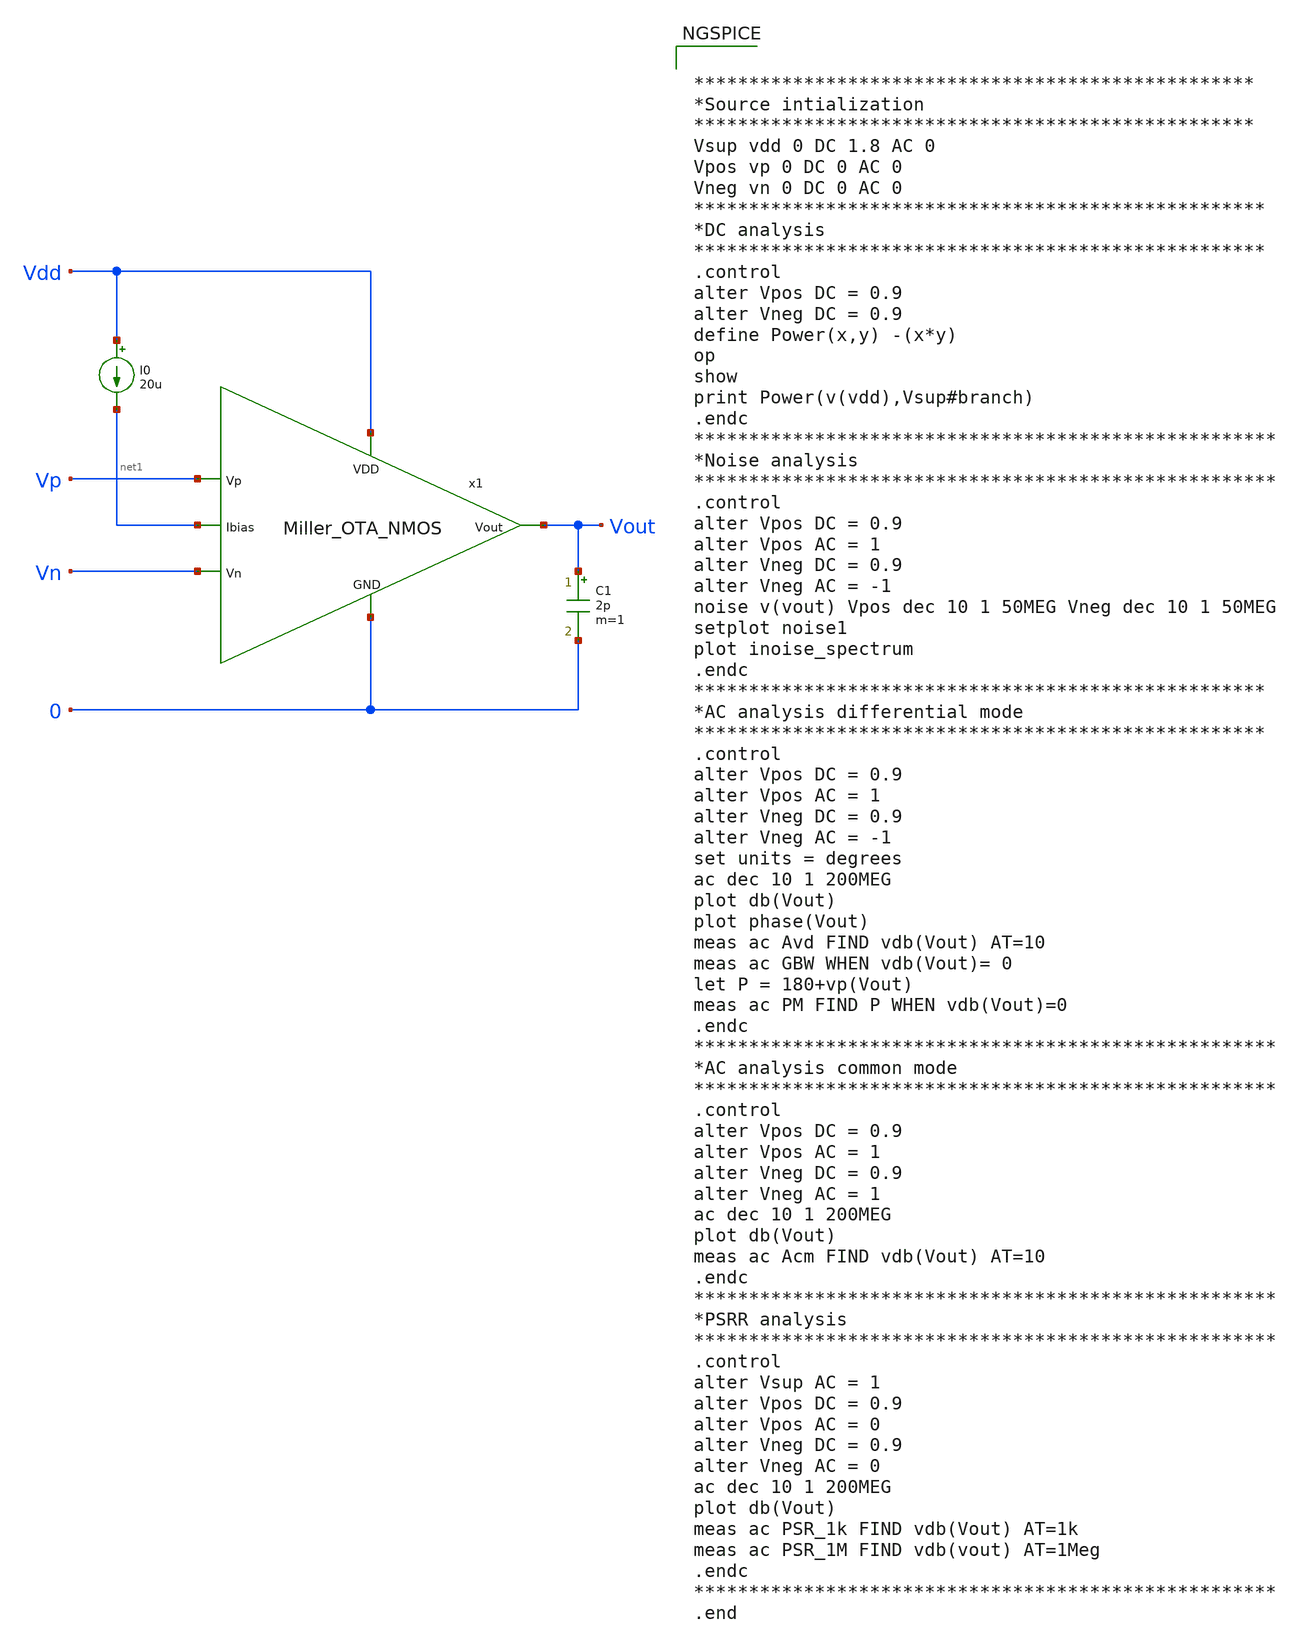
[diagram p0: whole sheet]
** sch_path: Analog_blocks/Analog_Blocks/OTA/Testbench/Miller_OTA/Transistor5v/Miller_OTA5v_meas.sch
**.subckt Miller_OTA5v_meas
I0 Vdd net1 20u
C1 Vout 0 2p m=1
x1 Vdd Vn Vp Vout net1 0 Miller_OTA_NMOS
**** begin user architecture code


***************************************************
*Source intialization
***************************************************
Vsup vdd 0 DC 1.8 AC 0
Vpos vp 0 DC 0 AC 0
Vneg vn 0 DC 0 AC 0
****************************************************
*DC analysis
****************************************************
.control
alter Vpos DC = 0.9
alter Vneg DC = 0.9
define Power(x,y) -(x*y)
op
show
print Power(v(vdd),Vsup#branch)
.endc
*****************************************************
*Noise analysis
*****************************************************
.control
alter Vpos DC = 0.9
alter Vpos AC = 1
alter Vneg DC = 0.9
alter Vneg AC = -1
noise v(vout) Vpos dec 10 1 50MEG Vneg dec 10 1 50MEG
setplot noise1
plot inoise_spectrum
.endc
****************************************************
*AC analysis differential mode
****************************************************
.control
alter Vpos DC = 0.9
alter Vpos AC = 1
alter Vneg DC = 0.9
alter Vneg AC = -1
set units = degrees
ac dec 10 1 200MEG
plot db(Vout)
plot phase(Vout)
meas ac Avd FIND vdb(Vout) AT=10
meas ac GBW WHEN vdb(Vout)= 0
let P = 180+vp(Vout)
meas ac PM FIND P WHEN vdb(Vout)=0
.endc
*****************************************************
*AC analysis common mode
*****************************************************
.control
alter Vpos DC = 0.9
alter Vpos AC = 1
alter Vneg DC = 0.9
alter Vneg AC = 1
ac dec 10 1 200MEG
plot db(Vout)
meas ac Acm FIND vdb(Vout) AT=10
.endc
*****************************************************
*PSRR analysis
*****************************************************
.control
alter Vsup AC = 1
alter Vpos DC = 0.9
alter Vpos AC = 0
alter Vneg DC = 0.9
alter Vneg AC = 0
ac dec 10 1 200MEG
plot db(Vout)
meas ac PSR_1k FIND vdb(Vout) AT=1k
meas ac PSR_1M FIND vdb(vout) AT=1Meg
.endc
*****************************************************
.end




.param mc_mm_switch=0
.param mc_pr_switch=0
.include ~/mabrains/Analog_blocks/models/sky130A/libs.ref/sky130_fd_pr/spice/sky130_fd_pr__nfet_01v8__tt.corner.spice
.include ~/mabrains/Analog_blocks/models/sky130A/libs.ref/sky130_fd_pr/spice/sky130_fd_pr__nfet_01v8_lvt__tt.corner.spice
.include ~/mabrains/Analog_blocks/models/sky130A/libs.ref/sky130_fd_pr/spice/sky130_fd_pr__pfet_01v8__tt.corner.spice
.include ~/mabrains/Analog_blocks/models/sky130A/libs.ref/sky130_fd_pr/spice/sky130_fd_pr__nfet_03v3_nvt__tt.corner.spice
.include ~/mabrains/Analog_blocks/models/sky130A/libs.ref/sky130_fd_pr/spice/sky130_fd_pr__nfet_05v0_nvt__tt.corner.spice
.include ~/mabrains/Analog_blocks/models/sky130A/libs.ref/sky130_fd_pr/spice/sky130_fd_pr__esd_nfet_01v8__tt.corner.spice
.include ~/mabrains/Analog_blocks/models/sky130A/libs.ref/sky130_fd_pr/spice/sky130_fd_pr__pfet_01v8_lvt__tt.corner.spice
.include ~/mabrains/Analog_blocks/models/sky130A/libs.ref/sky130_fd_pr/spice/sky130_fd_pr__pfet_01v8_hvt__tt.corner.spice
.include ~/mabrains/Analog_blocks/models/sky130A/libs.ref/sky130_fd_pr/spice/sky130_fd_pr__esd_pfet_g5v0d10v5__tt.corner.spice
.include ~/mabrains/Analog_blocks/models/sky130A/libs.ref/sky130_fd_pr/spice/sky130_fd_pr__pfet_g5v0d10v5__tt.corner.spice
.include ~/mabrains/Analog_blocks/models/sky130A/libs.ref/sky130_fd_pr/spice/sky130_fd_pr__pfet_g5v0d16v0__tt.corner.spice
.include ~/mabrains/Analog_blocks/models/sky130A/libs.ref/sky130_fd_pr/spice/sky130_fd_pr__nfet_g5v0d10v5__tt.corner.spice
.include ~/mabrains/Analog_blocks/models/sky130A/libs.ref/sky130_fd_pr/spice/sky130_fd_pr__nfet_g5v0d16v0__tt_discrete.corner.spice
.include ~/mabrains/Analog_blocks/models/sky130A/libs.ref/sky130_fd_pr/spice/sky130_fd_pr__esd_nfet_g5v0d10v5__tt.corner.spice
.include ~/mabrains/Analog_blocks/models/sky130A/libs.tech/ngspice/corners/tt/nonfet.spice
* Mismatch parameters
.include ~/mabrains/Analog_blocks/models/sky130A/libs.ref/sky130_fd_pr/spice/sky130_fd_pr__nfet_01v8__mismatch.corner.spice
.include ~/mabrains/Analog_blocks/models/sky130A/libs.ref/sky130_fd_pr/spice/sky130_fd_pr__pfet_01v8__mismatch.corner.spice
.include ~/mabrains/Analog_blocks/models/sky130A/libs.ref/sky130_fd_pr/spice/sky130_fd_pr__nfet_01v8_lvt__mismatch.corner.spice
.include ~/mabrains/Analog_blocks/models/sky130A/libs.ref/sky130_fd_pr/spice/sky130_fd_pr__pfet_01v8_lvt__mismatch.corner.spice
.include ~/mabrains/Analog_blocks/models/sky130A/libs.ref/sky130_fd_pr/spice/sky130_fd_pr__pfet_01v8_hvt__mismatch.corner.spice
.include ~/mabrains/Analog_blocks/models/sky130A/libs.ref/sky130_fd_pr/spice/sky130_fd_pr__nfet_g5v0d10v5__mismatch.corner.spice
.include ~/mabrains/Analog_blocks/models/sky130A/libs.ref/sky130_fd_pr/spice/sky130_fd_pr__pfet_g5v0d10v5__mismatch.corner.spice
.include ~/mabrains/Analog_blocks/models/sky130A/libs.ref/sky130_fd_pr/spice/sky130_fd_pr__nfet_05v0_nvt__mismatch.corner.spice
.include ~/mabrains/Analog_blocks/models/sky130A/libs.ref/sky130_fd_pr/spice/sky130_fd_pr__nfet_03v3_nvt__mismatch.corner.spice
* Resistor/Capacitor
.include ~/mabrains/Analog_blocks/models/sky130A/libs.tech/ngspice/r+c/res_typical__cap_typical.spice
.include ~/mabrains/Analog_blocks/models/sky130A/libs.tech/ngspice/r+c/res_typical__cap_typical__lin.spice
* Special cells
.include ~/mabrains/Analog_blocks/models/sky130A/libs.tech/ngspice/corners/tt/specialized_cells.spice
* All models
.include ~/mabrains/Analog_blocks/models/sky130A/libs.tech/ngspice/all.spice
* Corner
.include ~/mabrains/Analog_blocks/models/sky130A/libs.tech/ngspice/corners/tt/rf.spice



**** end user architecture code
**.ends

* expanding   symbol:
*+  /home/eslam/mabrains/Analog_blocks/Analog_Blocks/OTA/Schematic/Miller_OTA/Transistor5v/Miller_OTA_NMOS.sym # of pins=6
** sym_path: Analog_Blocks/OTA/Schematic/Miller_OTA/Transistor5v/Miller_OTA_NMOS.sym
** sch_path: Analog_Blocks/OTA/Schematic/Miller_OTA/Transistor5v/Miller_OTA_NMOS.sch
.subckt Miller_OTA_NMOS VDD Vn Vp Vout Ibias GND
*.ipin VDD
*.ipin Ibias
*.ipin Vn
*.ipin Vp
*.opin Vout
*.ipin GND
XM1 net1 Vn net3 GND sky130_fd_pr__nfet_g5v0d10v5 L=0.5 W=10 nf=1 ad='int((nf+1)/2) * W/nf * 0.29' as='int((nf+2)/2) * W/nf * 0.29'
+ pd='2*int((nf+1)/2) * (W/nf + 0.29)' ps='2*int((nf+2)/2) * (W/nf + 0.29)' nrd='0.29 / W' nrs='0.29 / W'
+ sa=0 sb=0 sd=0 mult=8 m=8
XM2 net2 Vp net3 GND sky130_fd_pr__nfet_g5v0d10v5 L=0.5 W=10 nf=1 ad='int((nf+1)/2) * W/nf * 0.29' as='int((nf+2)/2) * W/nf * 0.29'
+ pd='2*int((nf+1)/2) * (W/nf + 0.29)' ps='2*int((nf+2)/2) * (W/nf + 0.29)' nrd='0.29 / W' nrs='0.29 / W'
+ sa=0 sb=0 sd=0 mult=8 m=8
XM3 net1 net1 VDD VDD sky130_fd_pr__pfet_g5v0d10v5 L=0.5 W=5 nf=1 ad='int((nf+1)/2) * W/nf * 0.29' as='int((nf+2)/2) * W/nf * 0.29'
+ pd='2*int((nf+1)/2) * (W/nf + 0.29)' ps='2*int((nf+2)/2) * (W/nf + 0.29)' nrd='0.29 / W' nrs='0.29 / W'
+ sa=0 sb=0 sd=0 mult=4 m=4
XM4 net2 net1 VDD VDD sky130_fd_pr__pfet_g5v0d10v5 L=0.5 W=5 nf=1 ad='int((nf+1)/2) * W/nf * 0.29' as='int((nf+2)/2) * W/nf * 0.29'
+ pd='2*int((nf+1)/2) * (W/nf + 0.29)' ps='2*int((nf+2)/2) * (W/nf + 0.29)' nrd='0.29 / W' nrs='0.29 / W'
+ sa=0 sb=0 sd=0 mult=4 m=4
XM6 Vout net2 VDD VDD sky130_fd_pr__pfet_g5v0d10v5 L=0.5 W=5 nf=1 ad='int((nf+1)/2) * W/nf * 0.29' as='int((nf+2)/2) * W/nf * 0.29'
+ pd='2*int((nf+1)/2) * (W/nf + 0.29)' ps='2*int((nf+2)/2) * (W/nf + 0.29)' nrd='0.29 / W' nrs='0.29 / W'
+ sa=0 sb=0 sd=0 mult=20 m=20
XM5 net3 Ibias GND GND sky130_fd_pr__nfet_g5v0d10v5 L=1 W=3 nf=1 ad='int((nf+1)/2) * W/nf * 0.29' as='int((nf+2)/2) * W/nf * 0.29'
+ pd='2*int((nf+1)/2) * (W/nf + 0.29)' ps='2*int((nf+2)/2) * (W/nf + 0.29)' nrd='0.29 / W' nrs='0.29 / W'
+ sa=0 sb=0 sd=0 mult=8 m=8
XM8 Ibias Ibias GND GND sky130_fd_pr__nfet_g5v0d10v5 L=1 W=3 nf=1 ad='int((nf+1)/2) * W/nf * 0.29' as='int((nf+2)/2) * W/nf * 0.29'
+ pd='2*int((nf+1)/2) * (W/nf + 0.29)' ps='2*int((nf+2)/2) * (W/nf + 0.29)' nrd='0.29 / W' nrs='0.29 / W'
+ sa=0 sb=0 sd=0 mult=8 m=8
XC1 net2 Vout sky130_fd_pr__cap_mim_m3_2 W=25 L=25 MF=1 m=1
XM7 Vout Ibias GND GND sky130_fd_pr__nfet_g5v0d10v5 L=1 W=3 nf=1 ad='int((nf+1)/2) * W/nf * 0.29' as='int((nf+2)/2) * W/nf * 0.29'
+ pd='2*int((nf+1)/2) * (W/nf + 0.29)' ps='2*int((nf+2)/2) * (W/nf + 0.29)' nrd='0.29 / W' nrs='0.29 / W'
+ sa=0 sb=0 sd=0 mult=16 m=16
.ends

.end
